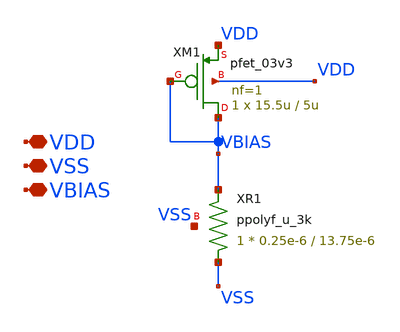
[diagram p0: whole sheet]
** sch_path: designs/pbias-gen.sch
**.subckt pbias-gen VDD VSS VBIAS
*.iopin VDD
*.iopin VSS
*.iopin VBIAS
XR1 VSS VBIAS VSS ppolyf_u_3k r_width=0.25e-6 r_length=13.75e-6 m=1
XM1 VBIAS VBIAS VDD VDD pfet_03v3 L=5u W=15.5u nf=1 ad='int((nf+1)/2) * W/nf * 0.18u' as='int((nf+2)/2) * W/nf * 0.18u'
+ pd='2*int((nf+1)/2) * (W/nf + 0.18u)' ps='2*int((nf+2)/2) * (W/nf + 0.18u)' nrd='0.18u / W' nrs='0.18u / W'
+ sa=0 sb=0 sd=0 m=1
**.ends
.end
